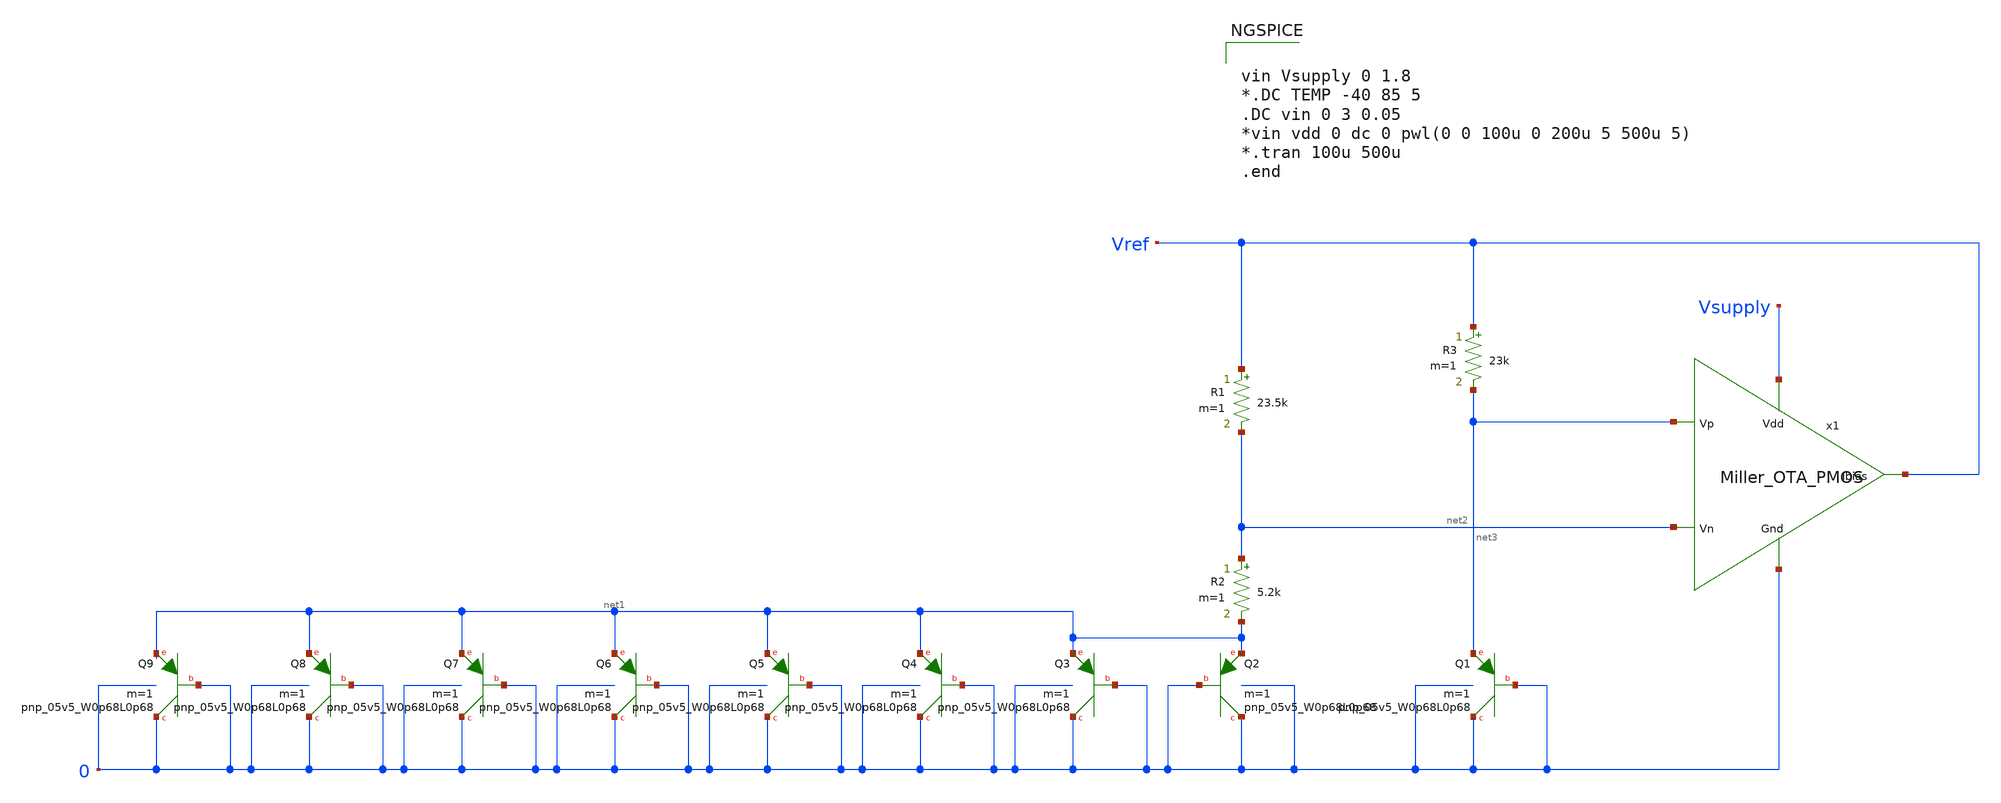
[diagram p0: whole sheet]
** sch_path: Bandgap/My Design/Schematics/Bandgap1.8v.sch
**.subckt Bandgap1.8v
R1 Vref net2 23.5k m=1
R2 net2 net1 5.2k m=1
R3 Vref net3 23k m=1
x1 Vsupply net3 net2 Vref 0 Miller_OTA_PMOS
XQ1 0 0 net3 sky130_fd_pr__pnp_05v5_W0p68L0p68 m=1
XQ2 0 0 net1 sky130_fd_pr__pnp_05v5_W0p68L0p68 m=1
XQ3 0 0 net1 sky130_fd_pr__pnp_05v5_W0p68L0p68 m=1
XQ4 0 0 net1 sky130_fd_pr__pnp_05v5_W0p68L0p68 m=1
XQ5 0 0 net1 sky130_fd_pr__pnp_05v5_W0p68L0p68 m=1
XQ6 0 0 net1 sky130_fd_pr__pnp_05v5_W0p68L0p68 m=1
XQ7 0 0 net1 sky130_fd_pr__pnp_05v5_W0p68L0p68 m=1
XQ8 0 0 net1 sky130_fd_pr__pnp_05v5_W0p68L0p68 m=1
XQ9 0 0 net1 sky130_fd_pr__pnp_05v5_W0p68L0p68 m=1
**** begin user architecture code


vin Vsupply 0 1.8
*.DC TEMP -40 85 5
.DC vin 0 3 0.05
*vin vdd 0 dc 0 pwl(0 0 100u 0 200u 5 500u 5)
*.tran 100u 500u
.end



.include $::SKYWATER_MODELS/cells/nfet_01v8/sky130_fd_pr__nfet_01v8__tt.corner.spice
.include $::SKYWATER_MODELS/cells/nfet_01v8_lvt/sky130_fd_pr__nfet_01v8_lvt__tt.corner.spice
.include $::SKYWATER_MODELS/cells/pfet_01v8/sky130_fd_pr__pfet_01v8__tt.corner.spice
.include $::SKYWATER_MODELS/cells/nfet_03v3_nvt/sky130_fd_pr__nfet_03v3_nvt__tt.corner.spice
.include $::SKYWATER_MODELS/cells/nfet_05v0_nvt/sky130_fd_pr__nfet_05v0_nvt__tt.corner.spice
.include $::SKYWATER_MODELS/cells/esd_nfet_01v8/sky130_fd_pr__esd_nfet_01v8__tt.corner.spice
.include $::SKYWATER_MODELS/cells/pfet_01v8_lvt/sky130_fd_pr__pfet_01v8_lvt__tt.corner.spice
.include $::SKYWATER_MODELS/cells/pfet_01v8_hvt/sky130_fd_pr__pfet_01v8_hvt__tt.corner.spice
.include $::SKYWATER_MODELS/cells/esd_pfet_g5v0d10v5/sky130_fd_pr__esd_pfet_g5v0d10v5__tt.corner.spice
.include $::SKYWATER_MODELS/cells/pfet_g5v0d10v5/sky130_fd_pr__pfet_g5v0d10v5__tt.corner.spice
.include $::SKYWATER_MODELS/cells/pfet_g5v0d16v0/sky130_fd_pr__pfet_g5v0d16v0__tt.corner.spice
.include $::SKYWATER_MODELS/cells/nfet_g5v0d10v5/sky130_fd_pr__nfet_g5v0d10v5__tt.corner.spice
.include $::SKYWATER_MODELS/cells/nfet_g5v0d16v0/sky130_fd_pr__nfet_g5v0d16v0__tt_discrete.corner.spice
.include $::SKYWATER_MODELS/cells/esd_nfet_g5v0d10v5/sky130_fd_pr__esd_nfet_g5v0d10v5__tt.corner.spice
.include $::SKYWATER_MODELS/models/corners/tt/nonfet.spice
* Mismatch parameters
.include $::SKYWATER_MODELS/cells/nfet_01v8/sky130_fd_pr__nfet_01v8__mismatch.corner.spice
.include $::SKYWATER_MODELS/cells/pfet_01v8/sky130_fd_pr__pfet_01v8__mismatch.corner.spice
.include $::SKYWATER_MODELS/cells/nfet_01v8_lvt/sky130_fd_pr__nfet_01v8_lvt__mismatch.corner.spice
.include $::SKYWATER_MODELS/cells/pfet_01v8_lvt/sky130_fd_pr__pfet_01v8_lvt__mismatch.corner.spice
.include $::SKYWATER_MODELS/cells/pfet_01v8_hvt/sky130_fd_pr__pfet_01v8_hvt__mismatch.corner.spice
.include $::SKYWATER_MODELS/cells/nfet_g5v0d10v5/sky130_fd_pr__nfet_g5v0d10v5__mismatch.corner.spice
.include $::SKYWATER_MODELS/cells/pfet_g5v0d10v5/sky130_fd_pr__pfet_g5v0d10v5__mismatch.corner.spice
.include $::SKYWATER_MODELS/cells/nfet_05v0_nvt/sky130_fd_pr__nfet_05v0_nvt__mismatch.corner.spice
.include $::SKYWATER_MODELS/cells/nfet_03v3_nvt/sky130_fd_pr__nfet_03v3_nvt__mismatch.corner.spice
* Resistor$::SKYWATER_MODELS/Capacitor
.include $::SKYWATER_MODELS/models/r+c/res_typical__cap_typical.spice
.include $::SKYWATER_MODELS/models/r+c/res_typical__cap_typical__lin.spice
* Special cells
.include $::SKYWATER_MODELS/models/corners/tt/specialized_cells.spice
* All models
.include $::SKYWATER_MODELS/models/all.spice
* Corner
.include $::SKYWATER_MODELS/models/corners/tt/rf.spice

**** end user architecture code
**.ends

* expanding   symbol:  /home/eslam/Analog_Design/OTA/Schematic/Miller_OTA_PMOS.sym # of pins=5
** sym_path: OTA/Schematic/Miller_OTA_PMOS.sym
** sch_path: OTA/Schematic/Miller_OTA_PMOS.sch
.subckt Miller_OTA_PMOS Vdd Vp Vn Ibias Gnd
*.ipin Vp
*.ipin Vn
*.opin Ibias
*.ipin Vdd
*.ipin Gnd
XM1 net2 Vp net3 Vdd sky130_fd_pr__pfet_01v8_lvt L=1 W=30 nf=1 ad='int((nf+1)/2) * W/nf * 0.29' as='int((nf+2)/2) * W/nf * 0.29'
+ pd='2*int((nf+1)/2) * (W/nf + 0.29)' ps='2*int((nf+2)/2) * (W/nf + 0.29)' nrd='0.29 / W' nrs='0.29 / W'
+ sa=0 sb=0 sd=0 mult=1 m=1
XM2 net1 Vn net3 Vdd sky130_fd_pr__pfet_01v8_lvt L=1 W=30 nf=1 ad='int((nf+1)/2) * W/nf * 0.29' as='int((nf+2)/2) * W/nf * 0.29'
+ pd='2*int((nf+1)/2) * (W/nf + 0.29)' ps='2*int((nf+2)/2) * (W/nf + 0.29)' nrd='0.29 / W' nrs='0.29 / W'
+ sa=0 sb=0 sd=0 mult=1 m=1
XM3 net2 net2 Gnd Gnd sky130_fd_pr__nfet_01v8_lvt L=0.5 W=7.4 nf=1 ad='int((nf+1)/2) * W/nf * 0.29' as='int((nf+2)/2) * W/nf * 0.29'
+ pd='2*int((nf+1)/2) * (W/nf + 0.29)' ps='2*int((nf+2)/2) * (W/nf + 0.29)' nrd='0.29 / W' nrs='0.29 / W'
+ sa=0 sb=0 sd=0 mult=1 m=1
XM4 net1 net2 Gnd Gnd sky130_fd_pr__nfet_01v8_lvt L=0.5 W=7.4 nf=1 ad='int((nf+1)/2) * W/nf * 0.29' as='int((nf+2)/2) * W/nf * 0.29'
+ pd='2*int((nf+1)/2) * (W/nf + 0.29)' ps='2*int((nf+2)/2) * (W/nf + 0.29)' nrd='0.29 / W' nrs='0.29 / W'
+ sa=0 sb=0 sd=0 mult=1 m=1
XM5 net3 net4 Vdd Vdd sky130_fd_pr__pfet_01v8_lvt L=1 W=10 nf=1 ad='int((nf+1)/2) * W/nf * 0.29' as='int((nf+2)/2) * W/nf * 0.29'
+ pd='2*int((nf+1)/2) * (W/nf + 0.29)' ps='2*int((nf+2)/2) * (W/nf + 0.29)' nrd='0.29 / W' nrs='0.29 / W'
+ sa=0 sb=0 sd=0 mult=1 m=1
XM6 Ibias net4 Vdd Vdd sky130_fd_pr__pfet_01v8_lvt L=1 W=10 nf=1 ad='int((nf+1)/2) * W/nf * 0.29' as='int((nf+2)/2) * W/nf * 0.29'
+ pd='2*int((nf+1)/2) * (W/nf + 0.29)' ps='2*int((nf+2)/2) * (W/nf + 0.29)' nrd='0.29 / W' nrs='0.29 / W'
+ sa=0 sb=0 sd=0 mult=1 m=1
XM7 net4 net4 Vdd Vdd sky130_fd_pr__pfet_01v8_lvt L=1 W=54 nf=1 ad='int((nf+1)/2) * W/nf * 0.29' as='int((nf+2)/2) * W/nf * 0.29'
+ pd='2*int((nf+1)/2) * (W/nf + 0.29)' ps='2*int((nf+2)/2) * (W/nf + 0.29)' nrd='0.29 / W' nrs='0.29 / W'
+ sa=0 sb=0 sd=0 mult=1 m=1
XM8 net4 net1 Gnd Gnd sky130_fd_pr__nfet_01v8_lvt L=0.5 W=75 nf=1 ad='int((nf+1)/2) * W/nf * 0.29' as='int((nf+2)/2) * W/nf * 0.29'
+ pd='2*int((nf+1)/2) * (W/nf + 0.29)' ps='2*int((nf+2)/2) * (W/nf + 0.29)' nrd='0.29 / W' nrs='0.29 / W'
+ sa=0 sb=0 sd=0 mult=1 m=1
C1 net1 net4 900f m=1
.ends

.end
